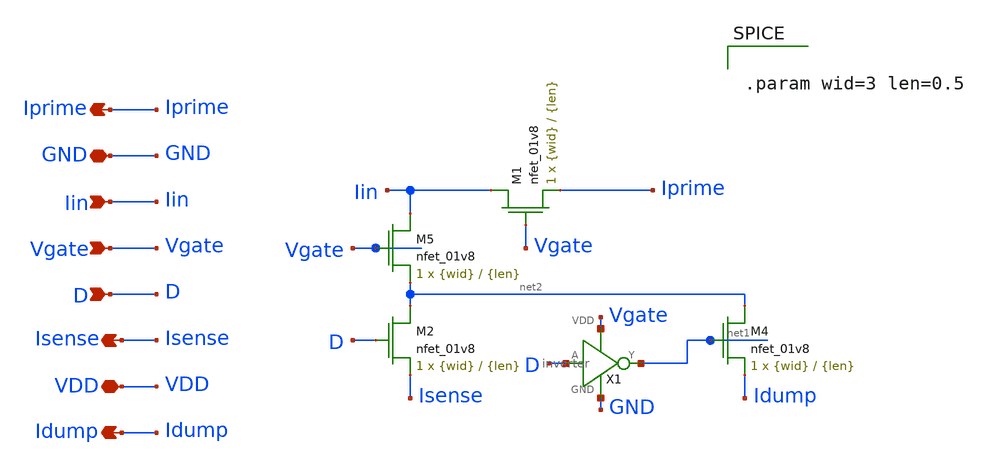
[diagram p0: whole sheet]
** sch_path: final/schematics/daccell.sch
**.subckt daccell GND VDD Isense Idump Iin Iprime Vgate D
*.iopin GND
*.iopin VDD
*.opin Isense
*.opin Idump
*.ipin Iin
*.opin Iprime
*.ipin Vgate
*.ipin D
XM5 Iin Vgate net2 GND sky130_fd_pr__nfet_01v8 L={len} W={wid} nf=1 ad='int((nf+1)/2) * W/nf * 0.29'
+ as='int((nf+2)/2) * W/nf * 0.29' pd='2*int((nf+1)/2) * (W/nf + 0.29)' ps='2*int((nf+2)/2) * (W/nf + 0.29)'
+ nrd='0.29 / W' nrs='0.29 / W' sa=0 sb=0 sd=0 mult=1 m=1
XM2 net2 D Isense GND sky130_fd_pr__nfet_01v8 L={len} W={wid} nf=1 ad='int((nf+1)/2) * W/nf * 0.29' as='int((nf+2)/2) * W/nf * 0.29'
+ pd='2*int((nf+1)/2) * (W/nf + 0.29)' ps='2*int((nf+2)/2) * (W/nf + 0.29)' nrd='0.29 / W' nrs='0.29 / W'
+ sa=0 sb=0 sd=0 mult=1 m=1
XM4 net2 net1 Idump GND sky130_fd_pr__nfet_01v8 L={len} W={wid} nf=1 ad='int((nf+1)/2) * W/nf * 0.29'
+ as='int((nf+2)/2) * W/nf * 0.29' pd='2*int((nf+1)/2) * (W/nf + 0.29)' ps='2*int((nf+2)/2) * (W/nf + 0.29)'
+ nrd='0.29 / W' nrs='0.29 / W' sa=0 sb=0 sd=0 mult=1 m=1
X1 Vgate D net1 GND inverter
XM1 Iin Vgate Iprime GND sky130_fd_pr__nfet_01v8 L={len} W={wid} nf=1 ad='int((nf+1)/2) * W/nf * 0.29'
+ as='int((nf+2)/2) * W/nf * 0.29' pd='2*int((nf+1)/2) * (W/nf + 0.29)' ps='2*int((nf+2)/2) * (W/nf + 0.29)'
+ nrd='0.29 / W' nrs='0.29 / W' sa=0 sb=0 sd=0 mult=1 m=1
**** begin user architecture code


.param wid=3 len=0.5


**** end user architecture code
**.ends

* expanding   symbol:  inverter.sym # of pins=4
** sym_path: final/schematics/inverter.sym
** sch_path: final/schematics/inverter.sch
.subckt inverter VDD A Y GND
*.ipin A
*.iopin VDD
*.iopin GND
*.opin Y
XM1 Y A GND GND sky130_fd_pr__nfet_01v8 L={len} W={wid} nf=1 ad='int((nf+1)/2) * W/nf * 0.29' as='int((nf+2)/2) * W/nf * 0.29'
+ pd='2*int((nf+1)/2) * (W/nf + 0.29)' ps='2*int((nf+2)/2) * (W/nf + 0.29)' nrd='0.29 / W' nrs='0.29 / W'
+ sa=0 sb=0 sd=0 mult=1 m=1
XM2 Y A VDD VDD sky130_fd_pr__pfet_01v8 L={len} W={wid} nf=1 ad='int((nf+1)/2) * W/nf * 0.29' as='int((nf+2)/2) * W/nf * 0.29'
+ pd='2*int((nf+1)/2) * (W/nf + 0.29)' ps='2*int((nf+2)/2) * (W/nf + 0.29)' nrd='0.29 / W' nrs='0.29 / W'
+ sa=0 sb=0 sd=0 mult=1 m=1
**** begin user architecture code


.param wid=3 len=0.5


**** end user architecture code
.ends

.end
